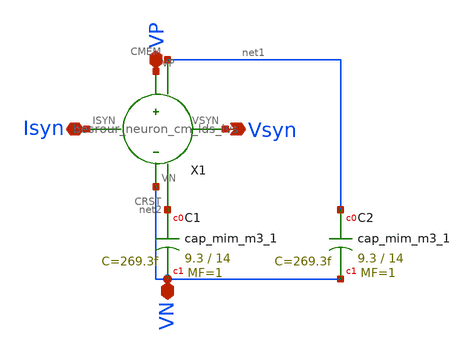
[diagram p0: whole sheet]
** sch_path: schematic/neuron_top_lvs.sch
**.subckt neuron_top_lvs VP VN Vsyn Isyn
*.iopin VP
*.iopin VN
*.opin Vsyn
*.iopin Isyn
X1 Isyn Vsyn VP VN net1 net2 besrour_neuron_cm_lds_lvs
XC1 net2 VN sky130_fd_pr__cap_mim_m3_1 W=9.3 L=14 MF=1 m=1
XC2 net1 VN sky130_fd_pr__cap_mim_m3_1 W=9.3 L=14 MF=1 m=1
**.ends

* expanding   symbol:
*+  /home/madvlsi/neuromorphic_computing_final/schematic/besrour_neuron_cm_lds_lvs.sym # of pins=6
** sym_path: schematic/besrour_neuron_cm_lds_lvs.sym
** sch_path: schematic/besrour_neuron_cm_lds_lvs.sch
.subckt besrour_neuron_cm_lds_lvs ISYN VSYN VP VN CMEM CRST
*.iopin VP
*.iopin VN
*.iopin ISYN
*.opin VSYN
*.opin CMEM
*.opin CRST
XM15 VP net1 net1 VP sky130_fd_pr__pfet_01v8 L=0.3 W=2 nf=1 ad='int((nf+1)/2) * W/nf * 0.29' as='int((nf+2)/2) * W/nf * 0.29'
+ pd='2*int((nf+1)/2) * (W/nf + 0.29)' ps='2*int((nf+2)/2) * (W/nf + 0.29)' nrd='0.29 / W' nrs='0.29 / W'
+ sa=0 sb=0 sd=0 mult=1 m=1
XM17 VN ISYN net1 VN sky130_fd_pr__nfet_01v8 L=0.3 W=2 nf=1 ad='int((nf+1)/2) * W/nf * 0.29' as='int((nf+2)/2) * W/nf * 0.29'
+ pd='2*int((nf+1)/2) * (W/nf + 0.29)' ps='2*int((nf+2)/2) * (W/nf + 0.29)' nrd='0.29 / W' nrs='0.29 / W'
+ sa=0 sb=0 sd=0 mult=1 m=1
XM7 ISYN ISYN VN VN sky130_fd_pr__nfet_01v8 L=0.3 W=2 nf=1 ad='int((nf+1)/2) * W/nf * 0.29' as='int((nf+2)/2) * W/nf * 0.29'
+ pd='2*int((nf+1)/2) * (W/nf + 0.29)' ps='2*int((nf+2)/2) * (W/nf + 0.29)' nrd='0.29 / W' nrs='0.29 / W'
+ sa=0 sb=0 sd=0 mult=1 m=1
XM8 VN CRST CMEM VN sky130_fd_pr__nfet_01v8 L=0.3 W=2 nf=1 ad='int((nf+1)/2) * W/nf * 0.29' as='int((nf+2)/2) * W/nf * 0.29'
+ pd='2*int((nf+1)/2) * (W/nf + 0.29)' ps='2*int((nf+2)/2) * (W/nf + 0.29)' nrd='0.29 / W' nrs='0.29 / W'
+ sa=0 sb=0 sd=0 mult=1 m=1
XM9 net2 CMEM VN VN sky130_fd_pr__nfet_01v8 L=0.3 W=2 nf=1 ad='int((nf+1)/2) * W/nf * 0.29' as='int((nf+2)/2) * W/nf * 0.29'
+ pd='2*int((nf+1)/2) * (W/nf + 0.29)' ps='2*int((nf+2)/2) * (W/nf + 0.29)' nrd='0.29 / W' nrs='0.29 / W'
+ sa=0 sb=0 sd=0 mult=1 m=1
XM10 VN net2 CRST VN sky130_fd_pr__nfet_01v8 L=0.3 W=2 nf=1 ad='int((nf+1)/2) * W/nf * 0.29' as='int((nf+2)/2) * W/nf * 0.29'
+ pd='2*int((nf+1)/2) * (W/nf + 0.29)' ps='2*int((nf+2)/2) * (W/nf + 0.29)' nrd='0.29 / W' nrs='0.29 / W'
+ sa=0 sb=0 sd=0 mult=1 m=1
XM11 net3 CRST VN VN sky130_fd_pr__nfet_01v8 L=0.3 W=2 nf=1 ad='int((nf+1)/2) * W/nf * 0.29' as='int((nf+2)/2) * W/nf * 0.29'
+ pd='2*int((nf+1)/2) * (W/nf + 0.29)' ps='2*int((nf+2)/2) * (W/nf + 0.29)' nrd='0.29 / W' nrs='0.29 / W'
+ sa=0 sb=0 sd=0 mult=1 m=1
XM12 VSYN net3 VN VN sky130_fd_pr__nfet_01v8 L=0.3 W=2 nf=1 ad='int((nf+1)/2) * W/nf * 0.29' as='int((nf+2)/2) * W/nf * 0.29'
+ pd='2*int((nf+1)/2) * (W/nf + 0.29)' ps='2*int((nf+2)/2) * (W/nf + 0.29)' nrd='0.29 / W' nrs='0.29 / W'
+ sa=0 sb=0 sd=0 mult=1 m=1
XM1 CMEM net1 VP VP sky130_fd_pr__pfet_01v8 L=0.3 W=2 nf=1 ad='int((nf+1)/2) * W/nf * 0.29' as='int((nf+2)/2) * W/nf * 0.29'
+ pd='2*int((nf+1)/2) * (W/nf + 0.29)' ps='2*int((nf+2)/2) * (W/nf + 0.29)' nrd='0.29 / W' nrs='0.29 / W'
+ sa=0 sb=0 sd=0 mult=1 m=1
XM2 VP net2 CMEM VP sky130_fd_pr__pfet_01v8 L=0.3 W=2 nf=1 ad='int((nf+1)/2) * W/nf * 0.29' as='int((nf+2)/2) * W/nf * 0.29'
+ pd='2*int((nf+1)/2) * (W/nf + 0.29)' ps='2*int((nf+2)/2) * (W/nf + 0.29)' nrd='0.29 / W' nrs='0.29 / W'
+ sa=0 sb=0 sd=0 mult=1 m=1
XM3 net2 CMEM VP VP sky130_fd_pr__pfet_01v8 L=0.3 W=2 nf=1 ad='int((nf+1)/2) * W/nf * 0.29' as='int((nf+2)/2) * W/nf * 0.29'
+ pd='2*int((nf+1)/2) * (W/nf + 0.29)' ps='2*int((nf+2)/2) * (W/nf + 0.29)' nrd='0.29 / W' nrs='0.29 / W'
+ sa=0 sb=0 sd=0 mult=1 m=1
XM4 VP net2 CRST VP sky130_fd_pr__pfet_01v8 L=0.3 W=2 nf=1 ad='int((nf+1)/2) * W/nf * 0.29' as='int((nf+2)/2) * W/nf * 0.29'
+ pd='2*int((nf+1)/2) * (W/nf + 0.29)' ps='2*int((nf+2)/2) * (W/nf + 0.29)' nrd='0.29 / W' nrs='0.29 / W'
+ sa=0 sb=0 sd=0 mult=1 m=1
XM5 net3 CRST VP VP sky130_fd_pr__pfet_01v8 L=0.3 W=2 nf=1 ad='int((nf+1)/2) * W/nf * 0.29' as='int((nf+2)/2) * W/nf * 0.29'
+ pd='2*int((nf+1)/2) * (W/nf + 0.29)' ps='2*int((nf+2)/2) * (W/nf + 0.29)' nrd='0.29 / W' nrs='0.29 / W'
+ sa=0 sb=0 sd=0 mult=1 m=1
XM6 VSYN net3 VP VP sky130_fd_pr__pfet_01v8 L=0.3 W=2 nf=1 ad='int((nf+1)/2) * W/nf * 0.29' as='int((nf+2)/2) * W/nf * 0.29'
+ pd='2*int((nf+1)/2) * (W/nf + 0.29)' ps='2*int((nf+2)/2) * (W/nf + 0.29)' nrd='0.29 / W' nrs='0.29 / W'
+ sa=0 sb=0 sd=0 mult=1 m=1
.ends

.end
